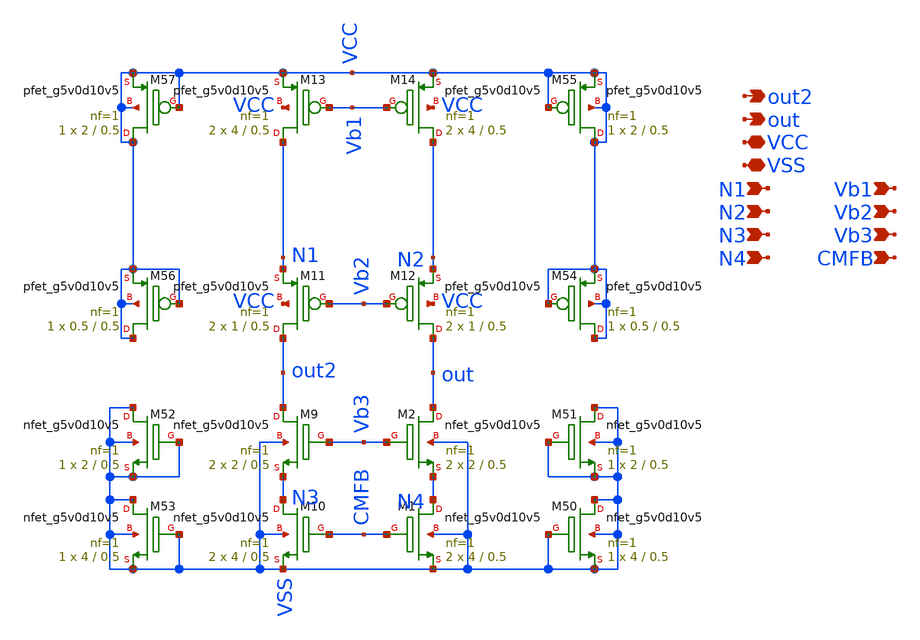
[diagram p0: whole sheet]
** sch_path: latest_working_comparator/folded_cascode.sch
**.subckt folded_cascode out VCC VSS N1 N2 N3 N4 out2 Vb1 Vb2 Vb3 CMFB
*.opin out
*.iopin VCC
*.iopin VSS
*.ipin N1
*.ipin N2
*.ipin N3
*.ipin N4
*.opin out2
*.ipin Vb1
*.ipin Vb2
*.ipin Vb3
*.ipin CMFB
XM1 N4 CMFB VSS VSS sky130_fd_pr__nfet_g5v0d10v5 L=0.5 W=4 nf=1 ad='int((nf+1)/2) * W/nf * 0.29' as='int((nf+2)/2) * W/nf * 0.29'
+ pd='2*int((nf+1)/2) * (W/nf + 0.29)' ps='2*int((nf+2)/2) * (W/nf + 0.29)' nrd='0.29 / W' nrs='0.29 / W'
+ sa=0 sb=0 sd=0 mult=2 m=2
XM2 out Vb3 N4 VSS sky130_fd_pr__nfet_g5v0d10v5 L=0.5 W=2 nf=1 ad='int((nf+1)/2) * W/nf * 0.29' as='int((nf+2)/2) * W/nf * 0.29'
+ pd='2*int((nf+1)/2) * (W/nf + 0.29)' ps='2*int((nf+2)/2) * (W/nf + 0.29)' nrd='0.29 / W' nrs='0.29 / W'
+ sa=0 sb=0 sd=0 mult=2 m=2
XM9 out2 Vb3 N3 VSS sky130_fd_pr__nfet_g5v0d10v5 L=0.5 W=2 nf=1 ad='int((nf+1)/2) * W/nf * 0.29' as='int((nf+2)/2) * W/nf * 0.29'
+ pd='2*int((nf+1)/2) * (W/nf + 0.29)' ps='2*int((nf+2)/2) * (W/nf + 0.29)' nrd='0.29 / W' nrs='0.29 / W'
+ sa=0 sb=0 sd=0 mult=2 m=2
XM10 N3 CMFB VSS VSS sky130_fd_pr__nfet_g5v0d10v5 L=0.5 W=4 nf=1 ad='int((nf+1)/2) * W/nf * 0.29' as='int((nf+2)/2) * W/nf * 0.29'
+ pd='2*int((nf+1)/2) * (W/nf + 0.29)' ps='2*int((nf+2)/2) * (W/nf + 0.29)' nrd='0.29 / W' nrs='0.29 / W'
+ sa=0 sb=0 sd=0 mult=2 m=2
XM11 out2 Vb2 N1 VCC sky130_fd_pr__pfet_g5v0d10v5 L=0.5 W=1 nf=1 ad='int((nf+1)/2) * W/nf * 0.29' as='int((nf+2)/2) * W/nf * 0.29'
+ pd='2*int((nf+1)/2) * (W/nf + 0.29)' ps='2*int((nf+2)/2) * (W/nf + 0.29)' nrd='0.29 / W' nrs='0.29 / W'
+ sa=0 sb=0 sd=0 mult=2 m=2
XM12 out Vb2 N2 VCC sky130_fd_pr__pfet_g5v0d10v5 L=0.5 W=1 nf=1 ad='int((nf+1)/2) * W/nf * 0.29' as='int((nf+2)/2) * W/nf * 0.29'
+ pd='2*int((nf+1)/2) * (W/nf + 0.29)' ps='2*int((nf+2)/2) * (W/nf + 0.29)' nrd='0.29 / W' nrs='0.29 / W'
+ sa=0 sb=0 sd=0 mult=2 m=2
XM13 N1 Vb1 VCC VCC sky130_fd_pr__pfet_g5v0d10v5 L=0.5 W=4 nf=1 ad='int((nf+1)/2) * W/nf * 0.29' as='int((nf+2)/2) * W/nf * 0.29'
+ pd='2*int((nf+1)/2) * (W/nf + 0.29)' ps='2*int((nf+2)/2) * (W/nf + 0.29)' nrd='0.29 / W' nrs='0.29 / W'
+ sa=0 sb=0 sd=0 mult=2 m=2
XM14 N2 Vb1 VCC VCC sky130_fd_pr__pfet_g5v0d10v5 L=0.5 W=4 nf=1 ad='int((nf+1)/2) * W/nf * 0.29' as='int((nf+2)/2) * W/nf * 0.29'
+ pd='2*int((nf+1)/2) * (W/nf + 0.29)' ps='2*int((nf+2)/2) * (W/nf + 0.29)' nrd='0.29 / W' nrs='0.29 / W'
+ sa=0 sb=0 sd=0 mult=2 m=2
XM50 VSS VSS VSS VSS sky130_fd_pr__nfet_g5v0d10v5 L=0.5 W=4 nf=1 ad='int((nf+1)/2) * W/nf * 0.29' as='int((nf+2)/2) * W/nf * 0.29'
+ pd='2*int((nf+1)/2) * (W/nf + 0.29)' ps='2*int((nf+2)/2) * (W/nf + 0.29)' nrd='0.29 / W' nrs='0.29 / W'
+ sa=0 sb=0 sd=0 mult=1 m=1
XM51 VSS VSS VSS VSS sky130_fd_pr__nfet_g5v0d10v5 L=0.5 W=2 nf=1 ad='int((nf+1)/2) * W/nf * 0.29' as='int((nf+2)/2) * W/nf * 0.29'
+ pd='2*int((nf+1)/2) * (W/nf + 0.29)' ps='2*int((nf+2)/2) * (W/nf + 0.29)' nrd='0.29 / W' nrs='0.29 / W'
+ sa=0 sb=0 sd=0 mult=1 m=1
XM52 VSS VSS VSS VSS sky130_fd_pr__nfet_g5v0d10v5 L=0.5 W=2 nf=1 ad='int((nf+1)/2) * W/nf * 0.29' as='int((nf+2)/2) * W/nf * 0.29'
+ pd='2*int((nf+1)/2) * (W/nf + 0.29)' ps='2*int((nf+2)/2) * (W/nf + 0.29)' nrd='0.29 / W' nrs='0.29 / W'
+ sa=0 sb=0 sd=0 mult=1 m=1
XM53 VSS VSS VSS VSS sky130_fd_pr__nfet_g5v0d10v5 L=0.5 W=4 nf=1 ad='int((nf+1)/2) * W/nf * 0.29' as='int((nf+2)/2) * W/nf * 0.29'
+ pd='2*int((nf+1)/2) * (W/nf + 0.29)' ps='2*int((nf+2)/2) * (W/nf + 0.29)' nrd='0.29 / W' nrs='0.29 / W'
+ sa=0 sb=0 sd=0 mult=1 m=1
XM54 VCC VCC VCC VCC sky130_fd_pr__pfet_g5v0d10v5 L=0.5 W=0.5 nf=1 ad='int((nf+1)/2) * W/nf * 0.29' as='int((nf+2)/2) * W/nf * 0.29'
+ pd='2*int((nf+1)/2) * (W/nf + 0.29)' ps='2*int((nf+2)/2) * (W/nf + 0.29)' nrd='0.29 / W' nrs='0.29 / W'
+ sa=0 sb=0 sd=0 mult=1 m=1
XM55 VCC VCC VCC VCC sky130_fd_pr__pfet_g5v0d10v5 L=0.5 W=2 nf=1 ad='int((nf+1)/2) * W/nf * 0.29' as='int((nf+2)/2) * W/nf * 0.29'
+ pd='2*int((nf+1)/2) * (W/nf + 0.29)' ps='2*int((nf+2)/2) * (W/nf + 0.29)' nrd='0.29 / W' nrs='0.29 / W'
+ sa=0 sb=0 sd=0 mult=1 m=1
XM56 VCC VCC VCC VCC sky130_fd_pr__pfet_g5v0d10v5 L=0.5 W=0.5 nf=1 ad='int((nf+1)/2) * W/nf * 0.29' as='int((nf+2)/2) * W/nf * 0.29'
+ pd='2*int((nf+1)/2) * (W/nf + 0.29)' ps='2*int((nf+2)/2) * (W/nf + 0.29)' nrd='0.29 / W' nrs='0.29 / W'
+ sa=0 sb=0 sd=0 mult=1 m=1
XM57 VCC VCC VCC VCC sky130_fd_pr__pfet_g5v0d10v5 L=0.5 W=2 nf=1 ad='int((nf+1)/2) * W/nf * 0.29' as='int((nf+2)/2) * W/nf * 0.29'
+ pd='2*int((nf+1)/2) * (W/nf + 0.29)' ps='2*int((nf+2)/2) * (W/nf + 0.29)' nrd='0.29 / W' nrs='0.29 / W'
+ sa=0 sb=0 sd=0 mult=1 m=1
**.ends
.end
